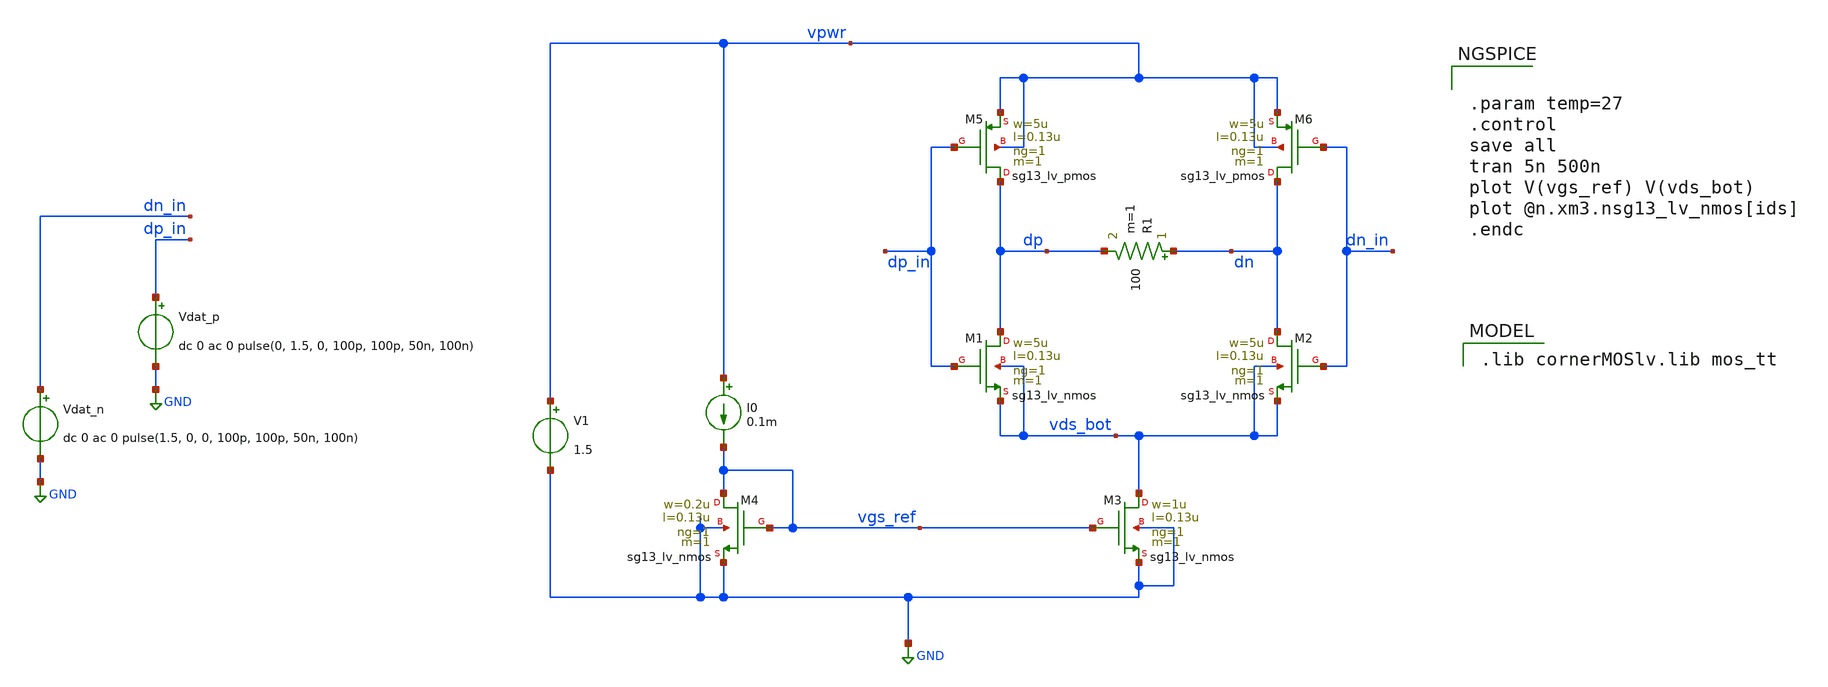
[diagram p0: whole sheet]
** sch_path: xschem/lvds_ideal_mirror_test.sch
**.subckt lvds_ideal_mirror_test
XM1 dp dp_in vds_bot vds_bot sg13_lv_nmos w=5u l=0.13u ng=1 m=1 mm_ok=1
XM2 dn dn_in vds_bot vds_bot sg13_lv_nmos w=5u l=0.13u ng=1 m=1 mm_ok=1
XM5 dp dp_in vpwr vpwr sg13_lv_pmos w=5u l=0.13u ng=1 m=1 mm_ok=1
XM6 dn dn_in vpwr vpwr sg13_lv_pmos w=5u l=0.13u ng=1 m=1 mm_ok=1
I0 vpwr vgs_ref 0.1m
XM3 vds_bot vgs_ref GND GND sg13_lv_nmos w=1u l=0.13u ng=1 m=1 mm_ok=1
XM4 vgs_ref vgs_ref GND GND sg13_lv_nmos w=0.2u l=0.13u ng=1 m=1 mm_ok=1
V1 vpwr GND 1.5
Vdat_p dp_in GND dc 0 ac 0 pulse(0, 1.5, 0, 100p, 100p, 50n, 100n)
Vdat_n dn_in GND dc 0 ac 0 pulse(1.5, 0, 0, 100p, 100p, 50n, 100n)
R1 dn dp 100 m=1
**** begin user architecture code
 .lib cornerMOSlv.lib mos_tt



.param temp=27
.control
save all
tran 5n 500n
plot V(vgs_ref) V(vds_bot)
plot @n.xm3.nsg13_lv_nmos[ids]
.endc


**** end user architecture code
**.ends
.GLOBAL GND
.end
